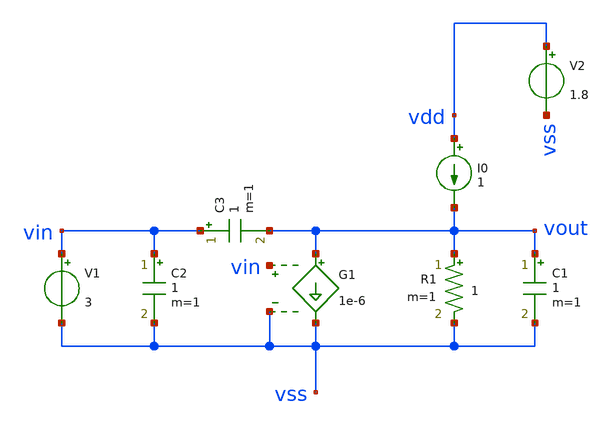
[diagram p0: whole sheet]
** sch_path: test-python/Tesis_notebooks/xschem/mna_example.sch
**.subckt mna_example
R1 vout vss 1 m=1
G1 vout vss vin vss 1e-6
C1 vout vss 1 m=1
I0 vdd vout 1
C2 vin vss 1 m=1
C3 vin vout 1 m=1
V1 vin vss 3
V2 vdd vss 1.8
**.ends
.end
